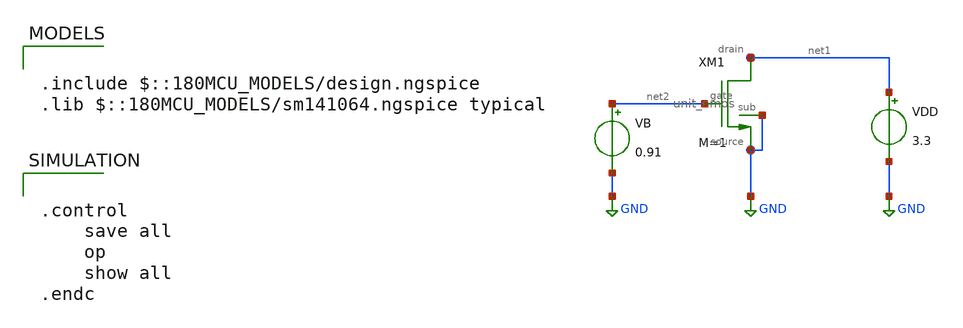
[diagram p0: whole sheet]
** sch_path: designs/libs/tb_single_mos/tb_single_nmos.sch
**.subckt tb_single_nmos
VB net2 GND 0.91
VDD net1 GND 3.3
XM1 net1 GND net2 GND unit_nmos M=1
**** begin user architecture code

.include $::180MCU_MODELS/design.ngspice
.lib $::180MCU_MODELS/sm141064.ngspice typical



.control
    save all
    op
    show all
.endc


**** end user architecture code
**.ends

* expanding   symbol:  libs/core_single_mos/unit_nmos/unit_nmos.sym # of pins=4
** sym_path: libs/core_single_mos/unit_nmos/unit_nmos.sym
** sch_path: libs/core_single_mos/unit_nmos/unit_nmos.sch
.subckt unit_nmos drain sub gate source
*.iopin drain
*.iopin source
*.iopin sub
*.iopin gate
XM1 drain gate source sub nfet_03v3 L=0.5u W=12u nf=2 ad='int((nf+1)/2) * W/nf * 0.18u' as='int((nf+2)/2) * W/nf * 0.18u'
+ pd='2*int((nf+1)/2) * (W/nf + 0.18u)' ps='2*int((nf+2)/2) * (W/nf + 0.18u)' nrd='0.18u / W' nrs='0.18u / W'
+ sa=0 sb=0 sd=0 m={M}
**** begin user architecture code

.param M=1

**** end user architecture code
.ends

.GLOBAL GND
.end
